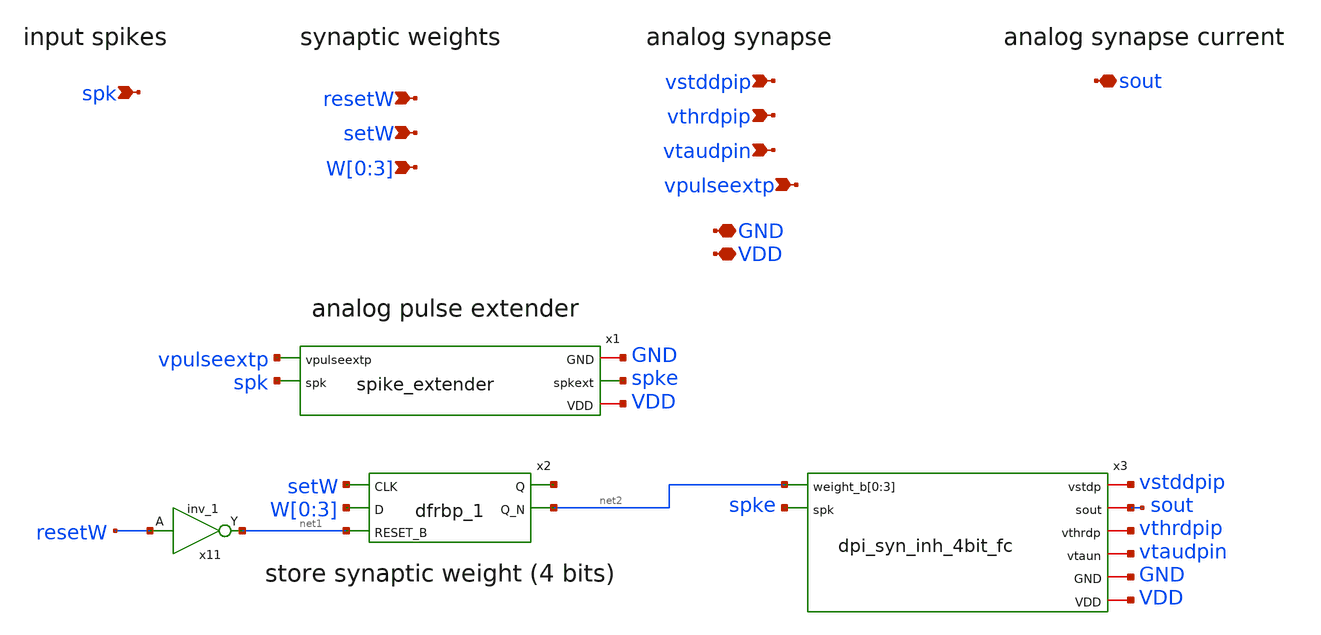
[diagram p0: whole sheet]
** sch_path: design/xschem/synapse_4bit_memory_inh.sch
**.subckt synapse_4bit_memory_inh GND VDD vpulseextp spk vthrdpip vtaudpin vstddpip
*+ W[0],W[1],W[2],W[3] setW resetW sout
*.iopin GND
*.iopin VDD
*.ipin vpulseextp
*.ipin spk
*.ipin vthrdpip
*.ipin vtaudpin
*.ipin vstddpip
*.ipin W[0],W[1],W[2],W[3]
*.ipin setW
*.ipin resetW
*.iopin sout
x1 vpulseextp spk GND spke VDD spike_extender
x11 resetW GND GND VDD VDD net1 sky130_fd_sc_hd__inv_1
x3 vstddpip net2 net2 net2 net2 spke sout vthrdpip vtaudpin GND VDD dpi_syn_inh_4bit_fc
x2 setW W[0] net1 GND GND VDD VDD net3 net2 sky130_fd_sc_hd__dfrbp_1
**.ends

* expanding   symbol:  spike_extender.sym # of pins=5
** sym_path: design/xschem/spike_extender.sym
** sch_path: design/xschem/spike_extender.sch
.subckt spike_extender vpulseextp spk GND spkext VDD
*.iopin GND
*.iopin VDD
*.ipin spk
*.opin spkext
*.ipin vpulseextp
XM1 net1 spk GND GND sky130_fd_pr__nfet_01v8 L=0.15 W=0.65 nf=1 ad='int((nf+1)/2) * W/nf * 0.29' as='int((nf+2)/2) * W/nf * 0.29'
+ pd='2*int((nf+1)/2) * (W/nf + 0.29)' ps='2*int((nf+2)/2) * (W/nf + 0.29)' nrd='0.29 / W' nrs='0.29 / W'
+ sa=0 sb=0 sd=0 mult=1 m=1
XM6 net1 vpulseextp VDD VDD sky130_fd_pr__pfet_01v8 L=2 W=1 nf=1 ad='int((nf+1)/2) * W/nf * 0.29' as='int((nf+2)/2) * W/nf * 0.29'
+ pd='2*int((nf+1)/2) * (W/nf + 0.29)' ps='2*int((nf+2)/2) * (W/nf + 0.29)' nrd='0.29 / W' nrs='0.29 / W'
+ sa=0 sb=0 sd=0 mult=1 m=1
XM5 net3 net2 GND GND sky130_fd_pr__nfet_01v8 L=0.15 W=0.65 nf=1 ad='int((nf+1)/2) * W/nf * 0.29' as='int((nf+2)/2) * W/nf * 0.29'
+ pd='2*int((nf+1)/2) * (W/nf + 0.29)' ps='2*int((nf+2)/2) * (W/nf + 0.29)' nrd='0.29 / W' nrs='0.29 / W'
+ sa=0 sb=0 sd=0 mult=1 m=1
XM8 spkext net3 GND GND sky130_fd_pr__nfet_01v8 L=0.15 W=0.65 nf=1 ad='int((nf+1)/2) * W/nf * 0.29' as='int((nf+2)/2) * W/nf * 0.29'
+ pd='2*int((nf+1)/2) * (W/nf + 0.29)' ps='2*int((nf+2)/2) * (W/nf + 0.29)' nrd='0.29 / W' nrs='0.29 / W'
+ sa=0 sb=0 sd=0 mult=1 m=1
XM4 net3 net2 VDD VDD sky130_fd_pr__pfet_01v8 L=0.15 W=1.0 nf=1 ad='int((nf+1)/2) * W/nf * 0.29' as='int((nf+2)/2) * W/nf * 0.29'
+ pd='2*int((nf+1)/2) * (W/nf + 0.29)' ps='2*int((nf+2)/2) * (W/nf + 0.29)' nrd='0.29 / W' nrs='0.29 / W'
+ sa=0 sb=0 sd=0 mult=1 m=1
XM7 spkext net3 VDD VDD sky130_fd_pr__pfet_01v8 L=0.15 W=1.0 nf=1 ad='int((nf+1)/2) * W/nf * 0.29' as='int((nf+2)/2) * W/nf * 0.29'
+ pd='2*int((nf+1)/2) * (W/nf + 0.29)' ps='2*int((nf+2)/2) * (W/nf + 0.29)' nrd='0.29 / W' nrs='0.29 / W'
+ sa=0 sb=0 sd=0 mult=1 m=1
XM2 net2 net1 GND GND sky130_fd_pr__nfet_01v8 L=0.15 W=0.65 nf=1 ad='int((nf+1)/2) * W/nf * 0.29' as='int((nf+2)/2) * W/nf * 0.29'
+ pd='2*int((nf+1)/2) * (W/nf + 0.29)' ps='2*int((nf+2)/2) * (W/nf + 0.29)' nrd='0.29 / W' nrs='0.29 / W'
+ sa=0 sb=0 sd=0 mult=1 m=1
XM3 net2 net1 VDD VDD sky130_fd_pr__pfet_01v8 L=0.15 W=1.0 nf=1 ad='int((nf+1)/2) * W/nf * 0.29' as='int((nf+2)/2) * W/nf * 0.29'
+ pd='2*int((nf+1)/2) * (W/nf + 0.29)' ps='2*int((nf+2)/2) * (W/nf + 0.29)' nrd='0.29 / W' nrs='0.29 / W'
+ sa=0 sb=0 sd=0 mult=1 m=1
XM9 GND net1 GND GND sky130_fd_pr__nfet_01v8 L=1 W=0.65 nf=1 ad='int((nf+1)/2) * W/nf * 0.29' as='int((nf+2)/2) * W/nf * 0.29'
+ pd='2*int((nf+1)/2) * (W/nf + 0.29)' ps='2*int((nf+2)/2) * (W/nf + 0.29)' nrd='0.29 / W' nrs='0.29 / W'
+ sa=0 sb=0 sd=0 mult=1 m=1
.ends


* expanding   symbol:  dpi_syn_inh_4bit_fc.sym # of pins=8
** sym_path: design/xschem/dpi_syn_inh_4bit_fc.sym
** sch_path: design/xschem/dpi_syn_inh_4bit_fc.sch
.subckt dpi_syn_inh_4bit_fc vstdp weight_b[0] weight_b[1] weight_b[2] weight_b[3] spk sout vthrdp
+ vtaun GND VDD
*.ipin spk
*.iopin vstdp
*.iopin vthrdp
*.iopin vtaun
*.iopin sout
*.iopin GND
*.iopin VDD
*.ipin weight_b[0],weight_b[1],weight_b[2],weight_b[3]
XM5 net2 net3 net1 VDD sky130_fd_pr__pfet_01v8 L=0.2 W=1.2 nf=1 ad='int((nf+1)/2) * W/nf * 0.29' as='int((nf+2)/2) * W/nf * 0.29'
+ pd='2*int((nf+1)/2) * (W/nf + 0.29)' ps='2*int((nf+2)/2) * (W/nf + 0.29)' nrd='0.29 / W' nrs='0.29 / W'
+ sa=0 sb=0 sd=0 mult=1 m=1
XM2 GND vthrdp net2 VDD sky130_fd_pr__pfet_01v8 L=0.2 W=1.2 nf=1 ad='int((nf+1)/2) * W/nf * 0.29' as='int((nf+2)/2) * W/nf * 0.29'
+ pd='2*int((nf+1)/2) * (W/nf + 0.29)' ps='2*int((nf+2)/2) * (W/nf + 0.29)' nrd='0.29 / W' nrs='0.29 / W'
+ sa=0 sb=0 sd=0 mult=1 m=1
XM3 vsin vsin net2 VDD sky130_fd_pr__pfet_01v8 L=0.2 W=1.2 nf=1 ad='int((nf+1)/2) * W/nf * 0.29' as='int((nf+2)/2) * W/nf * 0.29'
+ pd='2*int((nf+1)/2) * (W/nf + 0.29)' ps='2*int((nf+2)/2) * (W/nf + 0.29)' nrd='0.29 / W' nrs='0.29 / W'
+ sa=0 sb=0 sd=0 mult=1 m=1
XM4 vsin vtaun GND GND sky130_fd_pr__nfet_01v8 L=0.25 W=0.8 nf=1 ad='int((nf+1)/2) * W/nf * 0.29' as='int((nf+2)/2) * W/nf * 0.29'
+ pd='2*int((nf+1)/2) * (W/nf + 0.29)' ps='2*int((nf+2)/2) * (W/nf + 0.29)' nrd='0.29 / W' nrs='0.29 / W'
+ sa=0 sb=0 sd=0 mult=1 m=1
XM6 sout vsin net8 GND sky130_fd_pr__nfet_01v8 L=0.25 W=0.8 nf=1 ad='int((nf+1)/2) * W/nf * 0.29' as='int((nf+2)/2) * W/nf * 0.29'
+ pd='2*int((nf+1)/2) * (W/nf + 0.29)' ps='2*int((nf+2)/2) * (W/nf + 0.29)' nrd='0.29 / W' nrs='0.29 / W'
+ sa=0 sb=0 sd=0 mult=1 m=1
XM7 net3 spk GND GND sky130_fd_pr__nfet_01v8 L=0.25 W=0.8 nf=1 ad='int((nf+1)/2) * W/nf * 0.29' as='int((nf+2)/2) * W/nf * 0.29'
+ pd='2*int((nf+1)/2) * (W/nf + 0.29)' ps='2*int((nf+2)/2) * (W/nf + 0.29)' nrd='0.29 / W' nrs='0.29 / W'
+ sa=0 sb=0 sd=0 mult=1 m=1
XM8 net3 spk VDD VDD sky130_fd_pr__pfet_01v8 L=0.2 W=1.2 nf=1 ad='int((nf+1)/2) * W/nf * 0.29' as='int((nf+2)/2) * W/nf * 0.29'
+ pd='2*int((nf+1)/2) * (W/nf + 0.29)' ps='2*int((nf+2)/2) * (W/nf + 0.29)' nrd='0.29 / W' nrs='0.29 / W'
+ sa=0 sb=0 sd=0 mult=1 m=1
XC1 GND vsin sky130_fd_pr__cap_mim_m3_1 W=5 L=5 MF=1 m=1
XM9 net4 vstdp VDD VDD sky130_fd_pr__pfet_01v8 L=0.4 W=1.2 nf=1 ad='int((nf+1)/2) * W/nf * 0.29' as='int((nf+2)/2) * W/nf * 0.29'
+ pd='2*int((nf+1)/2) * (W/nf + 0.29)' ps='2*int((nf+2)/2) * (W/nf + 0.29)' nrd='0.29 / W' nrs='0.29 / W'
+ sa=0 sb=0 sd=0 mult=1 m=1
XM10 net1 weight_b[0] net4 VDD sky130_fd_pr__pfet_01v8 L=0.2 W=1.2 nf=1 ad='int((nf+1)/2) * W/nf * 0.29'
+ as='int((nf+2)/2) * W/nf * 0.29' pd='2*int((nf+1)/2) * (W/nf + 0.29)' ps='2*int((nf+2)/2) * (W/nf + 0.29)'
+ nrd='0.29 / W' nrs='0.29 / W' sa=0 sb=0 sd=0 mult=1 m=1
XM11 net1 weight_b[1] net5 VDD sky130_fd_pr__pfet_01v8 L=0.2 W=1.2 nf=1 ad='int((nf+1)/2) * W/nf * 0.29'
+ as='int((nf+2)/2) * W/nf * 0.29' pd='2*int((nf+1)/2) * (W/nf + 0.29)' ps='2*int((nf+2)/2) * (W/nf + 0.29)'
+ nrd='0.29 / W' nrs='0.29 / W' sa=0 sb=0 sd=0 mult=1 m=1
XM1 net5 vstdp VDD VDD sky130_fd_pr__pfet_01v8 L=1.5 W=1.2 nf=1 ad='int((nf+1)/2) * W/nf * 0.29' as='int((nf+2)/2) * W/nf * 0.29'
+ pd='2*int((nf+1)/2) * (W/nf + 0.29)' ps='2*int((nf+2)/2) * (W/nf + 0.29)' nrd='0.29 / W' nrs='0.29 / W'
+ sa=0 sb=0 sd=0 mult=1 m=1
XM12 net6 vstdp VDD VDD sky130_fd_pr__pfet_01v8 L=3.0 W=1.2 nf=1 ad='int((nf+1)/2) * W/nf * 0.29' as='int((nf+2)/2) * W/nf * 0.29'
+ pd='2*int((nf+1)/2) * (W/nf + 0.29)' ps='2*int((nf+2)/2) * (W/nf + 0.29)' nrd='0.29 / W' nrs='0.29 / W'
+ sa=0 sb=0 sd=0 mult=1 m=1
XM13 net7 vstdp VDD VDD sky130_fd_pr__pfet_01v8 L=6.0 W=1.2 nf=1 ad='int((nf+1)/2) * W/nf * 0.29' as='int((nf+2)/2) * W/nf * 0.29'
+ pd='2*int((nf+1)/2) * (W/nf + 0.29)' ps='2*int((nf+2)/2) * (W/nf + 0.29)' nrd='0.29 / W' nrs='0.29 / W'
+ sa=0 sb=0 sd=0 mult=1 m=1
XM14 net1 weight_b[2] net6 VDD sky130_fd_pr__pfet_01v8 L=0.2 W=1.2 nf=1 ad='int((nf+1)/2) * W/nf * 0.29'
+ as='int((nf+2)/2) * W/nf * 0.29' pd='2*int((nf+1)/2) * (W/nf + 0.29)' ps='2*int((nf+2)/2) * (W/nf + 0.29)'
+ nrd='0.29 / W' nrs='0.29 / W' sa=0 sb=0 sd=0 mult=1 m=1
XM15 net1 weight_b[3] net7 VDD sky130_fd_pr__pfet_01v8 L=0.2 W=1.2 nf=1 ad='int((nf+1)/2) * W/nf * 0.29'
+ as='int((nf+2)/2) * W/nf * 0.29' pd='2*int((nf+1)/2) * (W/nf + 0.29)' ps='2*int((nf+2)/2) * (W/nf + 0.29)'
+ nrd='0.29 / W' nrs='0.29 / W' sa=0 sb=0 sd=0 mult=1 m=1
Vmeas net8 GND 0
.save i(vmeas)
.ends

.end
